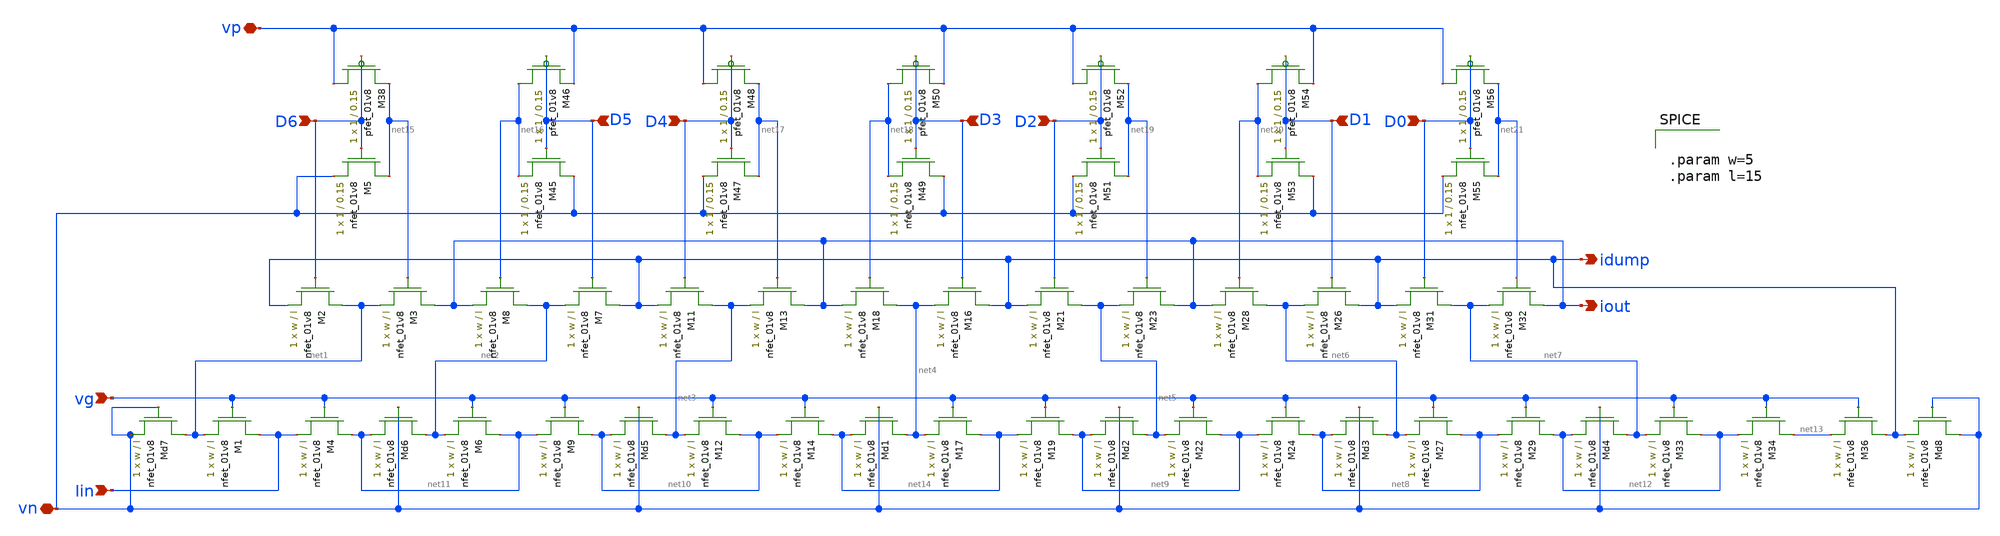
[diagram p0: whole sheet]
** sch_path: schematic/ladder_inverter_LDS.sch
**.subckt ladder_inverter_LDS iout idump vn vg D0 D1 D2 D3 D4 D5 D6 Iin vp
*.opin iout
*.opin idump
*.iopin vn
*.ipin vg
*.ipin D0
*.ipin D1
*.ipin D2
*.ipin D3
*.ipin D4
*.ipin D5
*.ipin D6
*.ipin Iin
*.iopin vp
XM1 Iin vg net1 GND sky130_fd_pr__nfet_01v8 L=l W=w nf=1 ad='int((nf+1)/2) * W/nf * 0.29' as='int((nf+2)/2) * W/nf * 0.29'
+ pd='2*int((nf+1)/2) * (W/nf + 0.29)' ps='2*int((nf+2)/2) * (W/nf + 0.29)' nrd='0.29 / W' nrs='0.29 / W'
+ sa=0 sb=0 sd=0 mult=1 m=1
XM2 net1 D6 idump GND sky130_fd_pr__nfet_01v8 L=l W=w nf=1 ad='int((nf+1)/2) * W/nf * 0.29' as='int((nf+2)/2) * W/nf * 0.29'
+ pd='2*int((nf+1)/2) * (W/nf + 0.29)' ps='2*int((nf+2)/2) * (W/nf + 0.29)' nrd='0.29 / W' nrs='0.29 / W'
+ sa=0 sb=0 sd=0 mult=1 m=1
XM3 iout net15 net1 GND sky130_fd_pr__nfet_01v8 L=l W=w nf=1 ad='int((nf+1)/2) * W/nf * 0.29' as='int((nf+2)/2) * W/nf * 0.29'
+ pd='2*int((nf+1)/2) * (W/nf + 0.29)' ps='2*int((nf+2)/2) * (W/nf + 0.29)' nrd='0.29 / W' nrs='0.29 / W'
+ sa=0 sb=0 sd=0 mult=1 m=1
XM4 net11 vg Iin GND sky130_fd_pr__nfet_01v8 L=l W=w nf=1 ad='int((nf+1)/2) * W/nf * 0.29' as='int((nf+2)/2) * W/nf * 0.29'
+ pd='2*int((nf+1)/2) * (W/nf + 0.29)' ps='2*int((nf+2)/2) * (W/nf + 0.29)' nrd='0.29 / W' nrs='0.29 / W'
+ sa=0 sb=0 sd=0 mult=1 m=1
XM6 net11 vg net2 GND sky130_fd_pr__nfet_01v8 L=l W=w nf=1 ad='int((nf+1)/2) * W/nf * 0.29' as='int((nf+2)/2) * W/nf * 0.29'
+ pd='2*int((nf+1)/2) * (W/nf + 0.29)' ps='2*int((nf+2)/2) * (W/nf + 0.29)' nrd='0.29 / W' nrs='0.29 / W'
+ sa=0 sb=0 sd=0 mult=1 m=1
XM7 idump D5 net2 GND sky130_fd_pr__nfet_01v8 L=l W=w nf=1 ad='int((nf+1)/2) * W/nf * 0.29' as='int((nf+2)/2) * W/nf * 0.29'
+ pd='2*int((nf+1)/2) * (W/nf + 0.29)' ps='2*int((nf+2)/2) * (W/nf + 0.29)' nrd='0.29 / W' nrs='0.29 / W'
+ sa=0 sb=0 sd=0 mult=1 m=1
XM8 net2 net16 iout GND sky130_fd_pr__nfet_01v8 L=l W=w nf=1 ad='int((nf+1)/2) * W/nf * 0.29' as='int((nf+2)/2) * W/nf * 0.29'
+ pd='2*int((nf+1)/2) * (W/nf + 0.29)' ps='2*int((nf+2)/2) * (W/nf + 0.29)' nrd='0.29 / W' nrs='0.29 / W'
+ sa=0 sb=0 sd=0 mult=1 m=1
XM9 net10 vg net11 GND sky130_fd_pr__nfet_01v8 L=l W=w nf=1 ad='int((nf+1)/2) * W/nf * 0.29' as='int((nf+2)/2) * W/nf * 0.29'
+ pd='2*int((nf+1)/2) * (W/nf + 0.29)' ps='2*int((nf+2)/2) * (W/nf + 0.29)' nrd='0.29 / W' nrs='0.29 / W'
+ sa=0 sb=0 sd=0 mult=1 m=1
XM11 net3 D4 idump GND sky130_fd_pr__nfet_01v8 L=l W=w nf=1 ad='int((nf+1)/2) * W/nf * 0.29' as='int((nf+2)/2) * W/nf * 0.29'
+ pd='2*int((nf+1)/2) * (W/nf + 0.29)' ps='2*int((nf+2)/2) * (W/nf + 0.29)' nrd='0.29 / W' nrs='0.29 / W'
+ sa=0 sb=0 sd=0 mult=1 m=1
XM12 net10 vg net3 GND sky130_fd_pr__nfet_01v8 L=l W=w nf=1 ad='int((nf+1)/2) * W/nf * 0.29' as='int((nf+2)/2) * W/nf * 0.29'
+ pd='2*int((nf+1)/2) * (W/nf + 0.29)' ps='2*int((nf+2)/2) * (W/nf + 0.29)' nrd='0.29 / W' nrs='0.29 / W'
+ sa=0 sb=0 sd=0 mult=1 m=1
XM13 iout net17 net3 GND sky130_fd_pr__nfet_01v8 L=l W=w nf=1 ad='int((nf+1)/2) * W/nf * 0.29' as='int((nf+2)/2) * W/nf * 0.29'
+ pd='2*int((nf+1)/2) * (W/nf + 0.29)' ps='2*int((nf+2)/2) * (W/nf + 0.29)' nrd='0.29 / W' nrs='0.29 / W'
+ sa=0 sb=0 sd=0 mult=1 m=1
XM14 net14 vg net10 GND sky130_fd_pr__nfet_01v8 L=l W=w nf=1 ad='int((nf+1)/2) * W/nf * 0.29' as='int((nf+2)/2) * W/nf * 0.29'
+ pd='2*int((nf+1)/2) * (W/nf + 0.29)' ps='2*int((nf+2)/2) * (W/nf + 0.29)' nrd='0.29 / W' nrs='0.29 / W'
+ sa=0 sb=0 sd=0 mult=1 m=1
XM16 idump D3 net4 GND sky130_fd_pr__nfet_01v8 L=l W=w nf=1 ad='int((nf+1)/2) * W/nf * 0.29' as='int((nf+2)/2) * W/nf * 0.29'
+ pd='2*int((nf+1)/2) * (W/nf + 0.29)' ps='2*int((nf+2)/2) * (W/nf + 0.29)' nrd='0.29 / W' nrs='0.29 / W'
+ sa=0 sb=0 sd=0 mult=1 m=1
XM17 net14 vg net4 GND sky130_fd_pr__nfet_01v8 L=l W=w nf=1 ad='int((nf+1)/2) * W/nf * 0.29' as='int((nf+2)/2) * W/nf * 0.29'
+ pd='2*int((nf+1)/2) * (W/nf + 0.29)' ps='2*int((nf+2)/2) * (W/nf + 0.29)' nrd='0.29 / W' nrs='0.29 / W'
+ sa=0 sb=0 sd=0 mult=1 m=1
XM18 net4 net18 iout GND sky130_fd_pr__nfet_01v8 L=l W=w nf=1 ad='int((nf+1)/2) * W/nf * 0.29' as='int((nf+2)/2) * W/nf * 0.29'
+ pd='2*int((nf+1)/2) * (W/nf + 0.29)' ps='2*int((nf+2)/2) * (W/nf + 0.29)' nrd='0.29 / W' nrs='0.29 / W'
+ sa=0 sb=0 sd=0 mult=1 m=1
XM19 net9 vg net14 GND sky130_fd_pr__nfet_01v8 L=l W=w nf=1 ad='int((nf+1)/2) * W/nf * 0.29' as='int((nf+2)/2) * W/nf * 0.29'
+ pd='2*int((nf+1)/2) * (W/nf + 0.29)' ps='2*int((nf+2)/2) * (W/nf + 0.29)' nrd='0.29 / W' nrs='0.29 / W'
+ sa=0 sb=0 sd=0 mult=1 m=1
XM21 net5 D2 idump GND sky130_fd_pr__nfet_01v8 L=l W=w nf=1 ad='int((nf+1)/2) * W/nf * 0.29' as='int((nf+2)/2) * W/nf * 0.29'
+ pd='2*int((nf+1)/2) * (W/nf + 0.29)' ps='2*int((nf+2)/2) * (W/nf + 0.29)' nrd='0.29 / W' nrs='0.29 / W'
+ sa=0 sb=0 sd=0 mult=1 m=1
XM22 net9 vg net5 GND sky130_fd_pr__nfet_01v8 L=l W=w nf=1 ad='int((nf+1)/2) * W/nf * 0.29' as='int((nf+2)/2) * W/nf * 0.29'
+ pd='2*int((nf+1)/2) * (W/nf + 0.29)' ps='2*int((nf+2)/2) * (W/nf + 0.29)' nrd='0.29 / W' nrs='0.29 / W'
+ sa=0 sb=0 sd=0 mult=1 m=1
XM23 iout net19 net5 GND sky130_fd_pr__nfet_01v8 L=l W=w nf=1 ad='int((nf+1)/2) * W/nf * 0.29' as='int((nf+2)/2) * W/nf * 0.29'
+ pd='2*int((nf+1)/2) * (W/nf + 0.29)' ps='2*int((nf+2)/2) * (W/nf + 0.29)' nrd='0.29 / W' nrs='0.29 / W'
+ sa=0 sb=0 sd=0 mult=1 m=1
XM24 net8 vg net9 GND sky130_fd_pr__nfet_01v8 L=l W=w nf=1 ad='int((nf+1)/2) * W/nf * 0.29' as='int((nf+2)/2) * W/nf * 0.29'
+ pd='2*int((nf+1)/2) * (W/nf + 0.29)' ps='2*int((nf+2)/2) * (W/nf + 0.29)' nrd='0.29 / W' nrs='0.29 / W'
+ sa=0 sb=0 sd=0 mult=1 m=1
XM26 idump D1 net6 GND sky130_fd_pr__nfet_01v8 L=l W=w nf=1 ad='int((nf+1)/2) * W/nf * 0.29' as='int((nf+2)/2) * W/nf * 0.29'
+ pd='2*int((nf+1)/2) * (W/nf + 0.29)' ps='2*int((nf+2)/2) * (W/nf + 0.29)' nrd='0.29 / W' nrs='0.29 / W'
+ sa=0 sb=0 sd=0 mult=1 m=1
XM27 net8 vg net6 GND sky130_fd_pr__nfet_01v8 L=l W=w nf=1 ad='int((nf+1)/2) * W/nf * 0.29' as='int((nf+2)/2) * W/nf * 0.29'
+ pd='2*int((nf+1)/2) * (W/nf + 0.29)' ps='2*int((nf+2)/2) * (W/nf + 0.29)' nrd='0.29 / W' nrs='0.29 / W'
+ sa=0 sb=0 sd=0 mult=1 m=1
XM28 net6 net20 iout GND sky130_fd_pr__nfet_01v8 L=l W=w nf=1 ad='int((nf+1)/2) * W/nf * 0.29' as='int((nf+2)/2) * W/nf * 0.29'
+ pd='2*int((nf+1)/2) * (W/nf + 0.29)' ps='2*int((nf+2)/2) * (W/nf + 0.29)' nrd='0.29 / W' nrs='0.29 / W'
+ sa=0 sb=0 sd=0 mult=1 m=1
XM29 net12 vg net8 GND sky130_fd_pr__nfet_01v8 L=l W=w nf=1 ad='int((nf+1)/2) * W/nf * 0.29' as='int((nf+2)/2) * W/nf * 0.29'
+ pd='2*int((nf+1)/2) * (W/nf + 0.29)' ps='2*int((nf+2)/2) * (W/nf + 0.29)' nrd='0.29 / W' nrs='0.29 / W'
+ sa=0 sb=0 sd=0 mult=1 m=1
XM31 net7 D0 idump GND sky130_fd_pr__nfet_01v8 L=l W=w nf=1 ad='int((nf+1)/2) * W/nf * 0.29' as='int((nf+2)/2) * W/nf * 0.29'
+ pd='2*int((nf+1)/2) * (W/nf + 0.29)' ps='2*int((nf+2)/2) * (W/nf + 0.29)' nrd='0.29 / W' nrs='0.29 / W'
+ sa=0 sb=0 sd=0 mult=1 m=1
XM32 iout net21 net7 GND sky130_fd_pr__nfet_01v8 L=l W=w nf=1 ad='int((nf+1)/2) * W/nf * 0.29' as='int((nf+2)/2) * W/nf * 0.29'
+ pd='2*int((nf+1)/2) * (W/nf + 0.29)' ps='2*int((nf+2)/2) * (W/nf + 0.29)' nrd='0.29 / W' nrs='0.29 / W'
+ sa=0 sb=0 sd=0 mult=1 m=1
XM33 net12 vg net7 GND sky130_fd_pr__nfet_01v8 L=l W=w nf=1 ad='int((nf+1)/2) * W/nf * 0.29' as='int((nf+2)/2) * W/nf * 0.29'
+ pd='2*int((nf+1)/2) * (W/nf + 0.29)' ps='2*int((nf+2)/2) * (W/nf + 0.29)' nrd='0.29 / W' nrs='0.29 / W'
+ sa=0 sb=0 sd=0 mult=1 m=1
XM34 net13 vg net12 GND sky130_fd_pr__nfet_01v8 L=l W=w nf=1 ad='int((nf+1)/2) * W/nf * 0.29' as='int((nf+2)/2) * W/nf * 0.29'
+ pd='2*int((nf+1)/2) * (W/nf + 0.29)' ps='2*int((nf+2)/2) * (W/nf + 0.29)' nrd='0.29 / W' nrs='0.29 / W'
+ sa=0 sb=0 sd=0 mult=1 m=1
XM36 idump vg net13 GND sky130_fd_pr__nfet_01v8 L=l W=w nf=1 ad='int((nf+1)/2) * W/nf * 0.29' as='int((nf+2)/2) * W/nf * 0.29'
+ pd='2*int((nf+1)/2) * (W/nf + 0.29)' ps='2*int((nf+2)/2) * (W/nf + 0.29)' nrd='0.29 / W' nrs='0.29 / W'
+ sa=0 sb=0 sd=0 mult=1 m=1
XMd1 net4 vn net14 GND sky130_fd_pr__nfet_01v8 L=l W=w nf=1 ad='int((nf+1)/2) * W/nf * 0.29' as='int((nf+2)/2) * W/nf * 0.29'
+ pd='2*int((nf+1)/2) * (W/nf + 0.29)' ps='2*int((nf+2)/2) * (W/nf + 0.29)' nrd='0.29 / W' nrs='0.29 / W'
+ sa=0 sb=0 sd=0 mult=1 m=1
XMd2 net5 vn net9 GND sky130_fd_pr__nfet_01v8 L=l W=w nf=1 ad='int((nf+1)/2) * W/nf * 0.29' as='int((nf+2)/2) * W/nf * 0.29'
+ pd='2*int((nf+1)/2) * (W/nf + 0.29)' ps='2*int((nf+2)/2) * (W/nf + 0.29)' nrd='0.29 / W' nrs='0.29 / W'
+ sa=0 sb=0 sd=0 mult=1 m=1
XMd3 net6 vn net8 GND sky130_fd_pr__nfet_01v8 L=l W=w nf=1 ad='int((nf+1)/2) * W/nf * 0.29' as='int((nf+2)/2) * W/nf * 0.29'
+ pd='2*int((nf+1)/2) * (W/nf + 0.29)' ps='2*int((nf+2)/2) * (W/nf + 0.29)' nrd='0.29 / W' nrs='0.29 / W'
+ sa=0 sb=0 sd=0 mult=1 m=1
XMd4 net7 vn net12 GND sky130_fd_pr__nfet_01v8 L=l W=w nf=1 ad='int((nf+1)/2) * W/nf * 0.29' as='int((nf+2)/2) * W/nf * 0.29'
+ pd='2*int((nf+1)/2) * (W/nf + 0.29)' ps='2*int((nf+2)/2) * (W/nf + 0.29)' nrd='0.29 / W' nrs='0.29 / W'
+ sa=0 sb=0 sd=0 mult=1 m=1
XMd5 net3 vn net10 GND sky130_fd_pr__nfet_01v8 L=l W=w nf=1 ad='int((nf+1)/2) * W/nf * 0.29' as='int((nf+2)/2) * W/nf * 0.29'
+ pd='2*int((nf+1)/2) * (W/nf + 0.29)' ps='2*int((nf+2)/2) * (W/nf + 0.29)' nrd='0.29 / W' nrs='0.29 / W'
+ sa=0 sb=0 sd=0 mult=1 m=1
XMd6 net2 vn net11 GND sky130_fd_pr__nfet_01v8 L=l W=w nf=1 ad='int((nf+1)/2) * W/nf * 0.29' as='int((nf+2)/2) * W/nf * 0.29'
+ pd='2*int((nf+1)/2) * (W/nf + 0.29)' ps='2*int((nf+2)/2) * (W/nf + 0.29)' nrd='0.29 / W' nrs='0.29 / W'
+ sa=0 sb=0 sd=0 mult=1 m=1
XMd7 net1 vn vn GND sky130_fd_pr__nfet_01v8 L=l W=w nf=1 ad='int((nf+1)/2) * W/nf * 0.29' as='int((nf+2)/2) * W/nf * 0.29'
+ pd='2*int((nf+1)/2) * (W/nf + 0.29)' ps='2*int((nf+2)/2) * (W/nf + 0.29)' nrd='0.29 / W' nrs='0.29 / W'
+ sa=0 sb=0 sd=0 mult=1 m=1
XMd8 vn vn idump GND sky130_fd_pr__nfet_01v8 L=l W=w nf=1 ad='int((nf+1)/2) * W/nf * 0.29' as='int((nf+2)/2) * W/nf * 0.29'
+ pd='2*int((nf+1)/2) * (W/nf + 0.29)' ps='2*int((nf+2)/2) * (W/nf + 0.29)' nrd='0.29 / W' nrs='0.29 / W'
+ sa=0 sb=0 sd=0 mult=1 m=1
XM5 net15 D6 vn GND sky130_fd_pr__nfet_01v8 L=0.15 W=1 nf=1 ad='int((nf+1)/2) * W/nf * 0.29' as='int((nf+2)/2) * W/nf * 0.29'
+ pd='2*int((nf+1)/2) * (W/nf + 0.29)' ps='2*int((nf+2)/2) * (W/nf + 0.29)' nrd='0.29 / W' nrs='0.29 / W'
+ sa=0 sb=0 sd=0 mult=1 m=1
XM38 vp D6 net15 VDD sky130_fd_pr__pfet_01v8 L=0.15 W=1 nf=1 ad='int((nf+1)/2) * W/nf * 0.29' as='int((nf+2)/2) * W/nf * 0.29'
+ pd='2*int((nf+1)/2) * (W/nf + 0.29)' ps='2*int((nf+2)/2) * (W/nf + 0.29)' nrd='0.29 / W' nrs='0.29 / W'
+ sa=0 sb=0 sd=0 mult=1 m=1
XM45 vn D5 net16 GND sky130_fd_pr__nfet_01v8 L=0.15 W=1 nf=1 ad='int((nf+1)/2) * W/nf * 0.29' as='int((nf+2)/2) * W/nf * 0.29'
+ pd='2*int((nf+1)/2) * (W/nf + 0.29)' ps='2*int((nf+2)/2) * (W/nf + 0.29)' nrd='0.29 / W' nrs='0.29 / W'
+ sa=0 sb=0 sd=0 mult=1 m=1
XM46 net16 D5 vp VDD sky130_fd_pr__pfet_01v8 L=0.15 W=1 nf=1 ad='int((nf+1)/2) * W/nf * 0.29' as='int((nf+2)/2) * W/nf * 0.29'
+ pd='2*int((nf+1)/2) * (W/nf + 0.29)' ps='2*int((nf+2)/2) * (W/nf + 0.29)' nrd='0.29 / W' nrs='0.29 / W'
+ sa=0 sb=0 sd=0 mult=1 m=1
XM47 net17 D4 vn GND sky130_fd_pr__nfet_01v8 L=0.15 W=1 nf=1 ad='int((nf+1)/2) * W/nf * 0.29' as='int((nf+2)/2) * W/nf * 0.29'
+ pd='2*int((nf+1)/2) * (W/nf + 0.29)' ps='2*int((nf+2)/2) * (W/nf + 0.29)' nrd='0.29 / W' nrs='0.29 / W'
+ sa=0 sb=0 sd=0 mult=1 m=1
XM48 vp D4 net17 VDD sky130_fd_pr__pfet_01v8 L=0.15 W=1 nf=1 ad='int((nf+1)/2) * W/nf * 0.29' as='int((nf+2)/2) * W/nf * 0.29'
+ pd='2*int((nf+1)/2) * (W/nf + 0.29)' ps='2*int((nf+2)/2) * (W/nf + 0.29)' nrd='0.29 / W' nrs='0.29 / W'
+ sa=0 sb=0 sd=0 mult=1 m=1
XM49 vn D3 net18 GND sky130_fd_pr__nfet_01v8 L=0.15 W=1 nf=1 ad='int((nf+1)/2) * W/nf * 0.29' as='int((nf+2)/2) * W/nf * 0.29'
+ pd='2*int((nf+1)/2) * (W/nf + 0.29)' ps='2*int((nf+2)/2) * (W/nf + 0.29)' nrd='0.29 / W' nrs='0.29 / W'
+ sa=0 sb=0 sd=0 mult=1 m=1
XM50 net18 D3 vp VDD sky130_fd_pr__pfet_01v8 L=0.15 W=1 nf=1 ad='int((nf+1)/2) * W/nf * 0.29' as='int((nf+2)/2) * W/nf * 0.29'
+ pd='2*int((nf+1)/2) * (W/nf + 0.29)' ps='2*int((nf+2)/2) * (W/nf + 0.29)' nrd='0.29 / W' nrs='0.29 / W'
+ sa=0 sb=0 sd=0 mult=1 m=1
XM51 net19 D2 vn GND sky130_fd_pr__nfet_01v8 L=0.15 W=1 nf=1 ad='int((nf+1)/2) * W/nf * 0.29' as='int((nf+2)/2) * W/nf * 0.29'
+ pd='2*int((nf+1)/2) * (W/nf + 0.29)' ps='2*int((nf+2)/2) * (W/nf + 0.29)' nrd='0.29 / W' nrs='0.29 / W'
+ sa=0 sb=0 sd=0 mult=1 m=1
XM52 vp D2 net19 VDD sky130_fd_pr__pfet_01v8 L=0.15 W=1 nf=1 ad='int((nf+1)/2) * W/nf * 0.29' as='int((nf+2)/2) * W/nf * 0.29'
+ pd='2*int((nf+1)/2) * (W/nf + 0.29)' ps='2*int((nf+2)/2) * (W/nf + 0.29)' nrd='0.29 / W' nrs='0.29 / W'
+ sa=0 sb=0 sd=0 mult=1 m=1
XM53 vn D1 net20 GND sky130_fd_pr__nfet_01v8 L=0.15 W=1 nf=1 ad='int((nf+1)/2) * W/nf * 0.29' as='int((nf+2)/2) * W/nf * 0.29'
+ pd='2*int((nf+1)/2) * (W/nf + 0.29)' ps='2*int((nf+2)/2) * (W/nf + 0.29)' nrd='0.29 / W' nrs='0.29 / W'
+ sa=0 sb=0 sd=0 mult=1 m=1
XM54 net20 D1 vp VDD sky130_fd_pr__pfet_01v8 L=0.15 W=1 nf=1 ad='int((nf+1)/2) * W/nf * 0.29' as='int((nf+2)/2) * W/nf * 0.29'
+ pd='2*int((nf+1)/2) * (W/nf + 0.29)' ps='2*int((nf+2)/2) * (W/nf + 0.29)' nrd='0.29 / W' nrs='0.29 / W'
+ sa=0 sb=0 sd=0 mult=1 m=1
XM55 net21 D0 vn GND sky130_fd_pr__nfet_01v8 L=0.15 W=1 nf=1 ad='int((nf+1)/2) * W/nf * 0.29' as='int((nf+2)/2) * W/nf * 0.29'
+ pd='2*int((nf+1)/2) * (W/nf + 0.29)' ps='2*int((nf+2)/2) * (W/nf + 0.29)' nrd='0.29 / W' nrs='0.29 / W'
+ sa=0 sb=0 sd=0 mult=1 m=1
XM56 vp D0 net21 VDD sky130_fd_pr__pfet_01v8 L=0.15 W=1 nf=1 ad='int((nf+1)/2) * W/nf * 0.29' as='int((nf+2)/2) * W/nf * 0.29'
+ pd='2*int((nf+1)/2) * (W/nf + 0.29)' ps='2*int((nf+2)/2) * (W/nf + 0.29)' nrd='0.29 / W' nrs='0.29 / W'
+ sa=0 sb=0 sd=0 mult=1 m=1
**** begin user architecture code


.param w=5
.param l=15


**** end user architecture code
**.ends
.end
